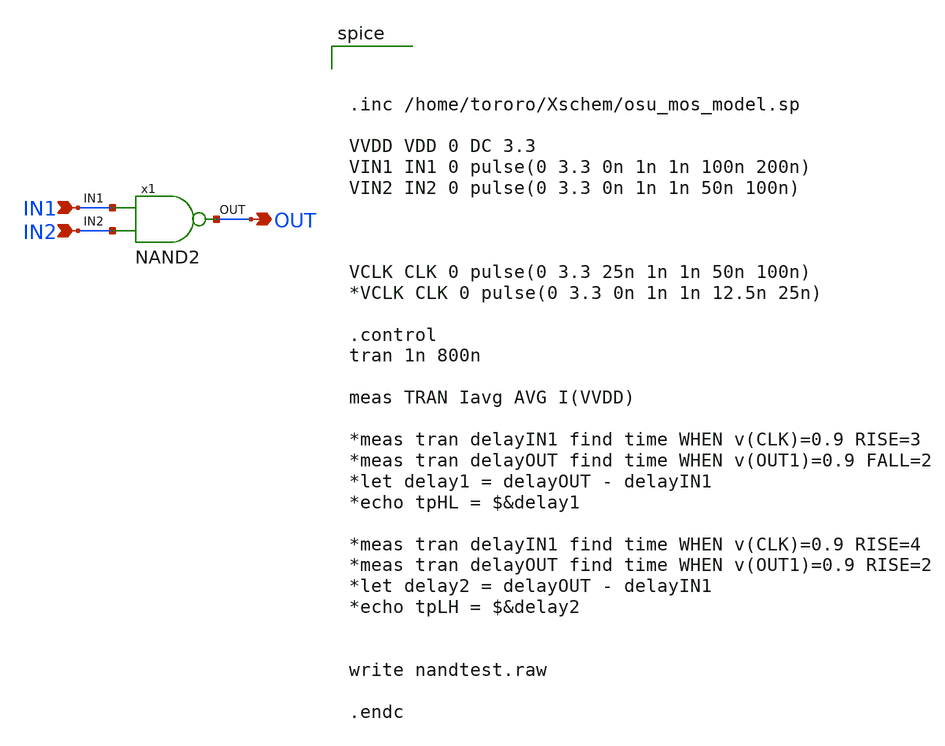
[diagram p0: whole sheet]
** sch_path: LR_hokari/LR_Work2/nandtest.sch
**.subckt nandtest IN1 IN2 OUT
*.ipin IN1
*.ipin IN2
*.opin OUT
x1 OUT IN1 IN2 NAND2
**** begin user architecture code



.inc /home/tororo/Xschem/osu_mos_model.sp

VVDD VDD 0 DC 3.3
VIN1 IN1 0 pulse(0 3.3 0n 1n 1n 100n 200n)
VIN2 IN2 0 pulse(0 3.3 0n 1n 1n 50n 100n)



VCLK CLK 0 pulse(0 3.3 25n 1n 1n 50n 100n)
*VCLK CLK 0 pulse(0 3.3 0n 1n 1n 12.5n 25n)

.control
tran 1n 800n

meas TRAN Iavg AVG I(VVDD)

*meas tran delayIN1 find time WHEN v(CLK)=0.9 RISE=3
*meas tran delayOUT find time WHEN v(OUT1)=0.9 FALL=2
*let delay1 = delayOUT - delayIN1
*echo tpHL = $&delay1

*meas tran delayIN1 find time WHEN v(CLK)=0.9 RISE=4
*meas tran delayOUT find time WHEN v(OUT1)=0.9 RISE=2
*let delay2 = delayOUT - delayIN1
*echo tpLH = $&delay2


write nandtest.raw

.endc

**** end user architecture code
**.ends
.end
